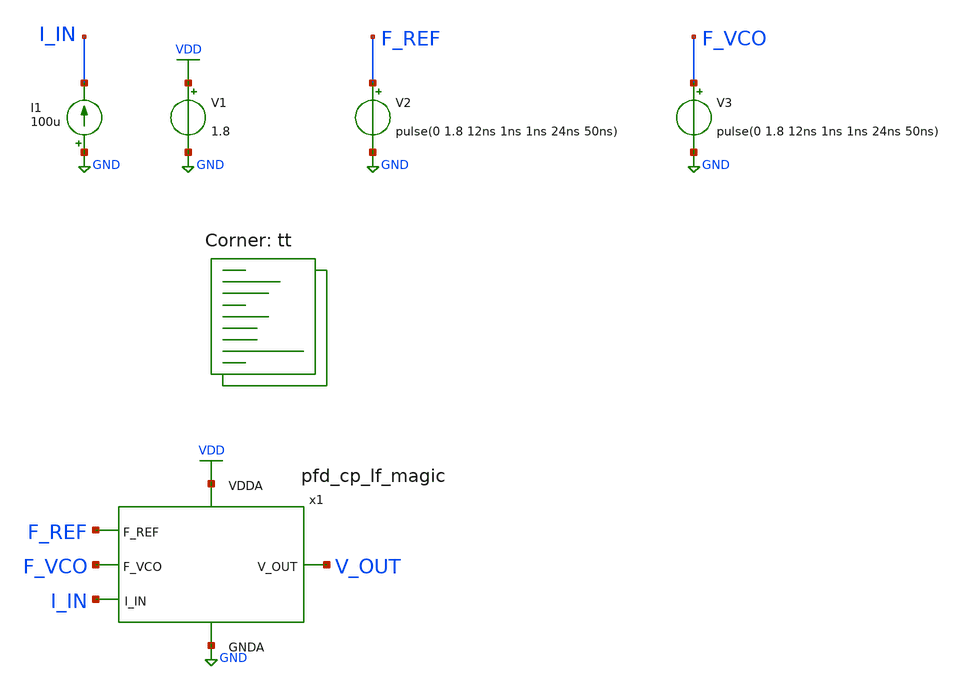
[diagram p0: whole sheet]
** sch_path: projects/pll/charge_pump/magic/pfd_charge_pump_magic_4.sch
**.subckt pfd_charge_pump_magic_4
V1 VDD GND 1.8
V2 F_REF GND pulse(0 1.8 12ns 1ns 1ns 24ns 50ns)
V3 F_VCO GND pulse(0 1.8 12ns 1ns 1ns 24ns 50ns)
I1 GND I_IN 100u
x1 V_OUT VDD GND F_REF F_VCO I_IN pfd_cp_lf_magic
**** begin user architecture code
.lib $::SKYWATER_MODELS/sky130.lib.spice tt



.include /foss/designs/my_design/projects/pll/full_pll/magic/pfd_cp_lf_magic.spice

.option method=gear
.option wnflag=1
* .option savecurrents

.save @m.x1.x24.msky130_fd_pr__pfet_01v8[id] @m.x1.x44.msky130_fd_pr__pfet_01v8[id] @m.x1.x62.msky130_fd_pr__pfet_01v8[id] @m.x1.x75.msky130_fd_pr__pfet_01v8[id] @m.x1.x124.msky130_fd_pr__nfet_01v8[id] @m.x1.x139.msky130_fd_pr__nfet_01v8[id] v(x1.pfd_8_0.up_pfd.t0) v(x1.pfd_8_0.up_pfd_b.t0) v(x1.pfd_8_0.down_pfd.t0) v(x1.pfd_8_0.down_pfd_b.t0) v(x1.pfd_8_0.up.t0) v(x1.pfd_8_0.up_b.t0) v(x1.pfd_8_0.down.t0) v(x1.pfd_8_0.down_b.t0) v(x1.charge_pump_cell_6_0.x.t0) v(x1.pfd_8_0.opamp_out.t0) v(x1.charge_pump_cell_6_0.up_input.t0) v(x1.charge_pump_cell_6_0.down_input.t0) v(x1.charge_pump_cell_6_0.down_gate.t0) v(f_ref) v(f_vco) v(i_in) v(v_out)


* V_out initial voltage value for the F_VCO delay of 2ns  (leading)
* .ic v(v_out) = 1.8

* V_out initial voltage value for the F_VCO delay of 12ns (lock condition)
.ic v(v_out) = 0.9

* V_out initial voltage value for the F_VCO delay of 22ns (lagging)
* .ic v(v_out) = 0.0

.control
  * save v(f_ref) v(f_vco) v(i_in) v(v_out)
  * save all

  * timestep for exact simulation results
  * tran 5ps 0.5us

  * timestep for faster simulation results
  tran 50ps 0.02us

  remzerovec
  write pfd_charge_pump_magic_4_2.raw
  set appendwrite

.endc



**** end user architecture code
**.ends
.GLOBAL GND
.GLOBAL VDD
.end
